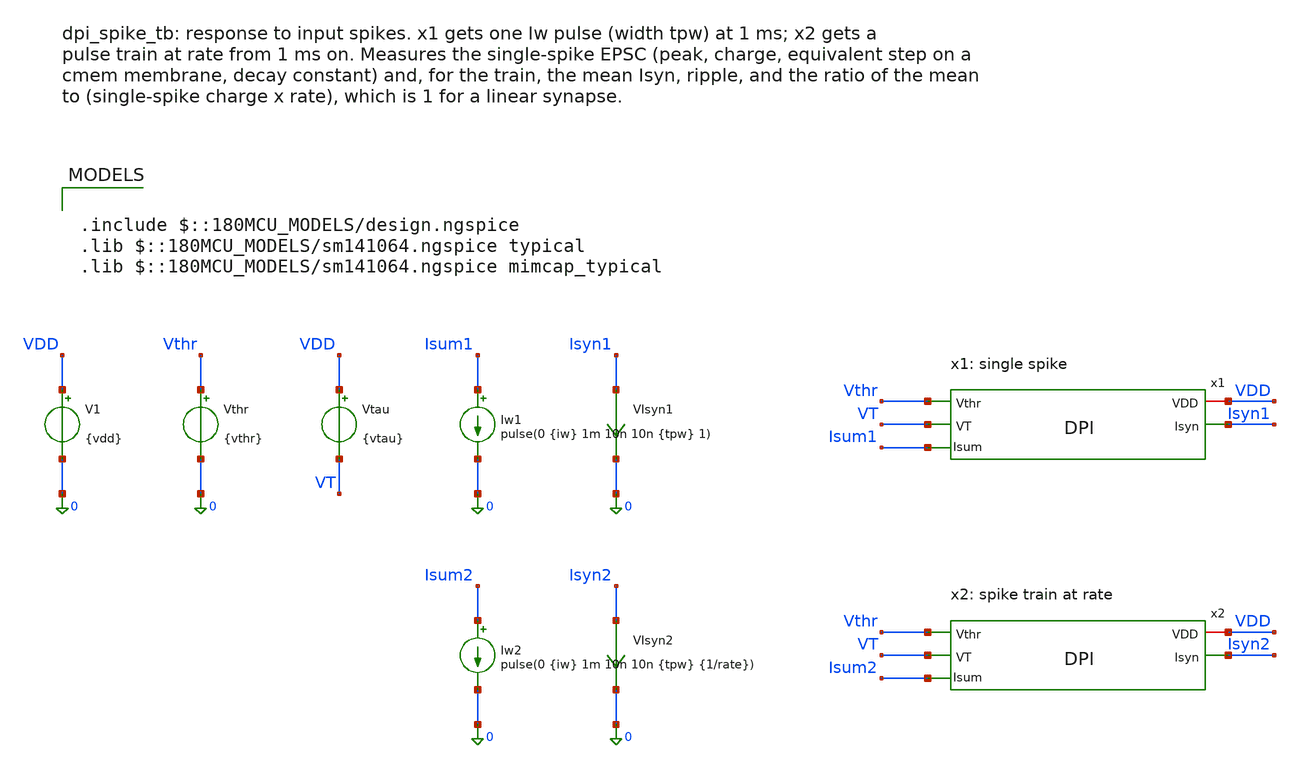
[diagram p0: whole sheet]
** sch_path: analog/testbenches/dpi/dpi_spike_tb.sch
**.subckt dpi_spike_tb
V1 VDD 0 {vdd}
Vthr Vthr 0 {vthr}
Vtau VDD VT {vtau}
Iw1 Isum1 0 pulse(0 {iw} 1m 10n 10n {tpw} 1)
VIsyn1 Isyn1 0 0
.save i(visyn1)
Iw2 Isum2 0 pulse(0 {iw} 1m 10n 10n {tpw} {1/rate})
VIsyn2 Isyn2 0 0
.save i(visyn2)
x1 VDD Vthr Isyn1 Isum1 VT DPI
x2 VDD Vthr Isyn2 Isum2 VT DPI
**** begin user architecture code


* Reference operating point (see analog/testbenches/README.md)
* cmem is only used to convert charge per spike into a membrane step (neuron_5khz Cmem)
.param vdd=3.3 vthr=2.9 vtau=0.40 iw=5n tpw=100u rate=1k cmem=0.86p
.csparam iw_c={iw}
.csparam tpw_c={tpw}
.csparam rate_c={rate}
.csparam cmem_c={cmem}
.control
  save all
  set wr_singlescale
  set wr_vecnames
  tran 0.5u 21m 0 1u
  let isyn1 = i(VIsyn1)
  let isyn2 = i(VIsyn2)

  * Single spike (x1)
  meas tran i_base find isyn1 at=0.9m
  meas tran ipk1 max isyn1 from=1m to=11m
  meas tran q1 integ isyn1 from=1m to=11m
  let q1 = q1 - i_base*10m
  let dv_mem = q1/cmem_c
  let t_end = 1m + tpw_c
  let l37 = i_base + 0.3679*(ipk1 - i_base)
  meas tran t37 when isyn1=$&l37 fall=1 td=$&t_end
  let tau_epsc = t37 - t_end

  * Spike train (x2), measured once settled
  meas tran iavg2 avg isyn2 from=11m to=21m
  meas tran imax2 max isyn2 from=11m to=21m
  meas tran imin2 min isyn2 from=11m to=21m
  let ripple = (imax2 - imin2)/iavg2
  let lin_rate = (iavg2 - i_base)/(q1*rate_c)
  let pk_ratio = imax2/ipk1

  echo RES ipk1=$&ipk1
  echo RES q1=$&q1
  echo RES dv_mem=$&dv_mem
  echo RES tau_epsc=$&tau_epsc
  echo RES iavg2=$&iavg2
  echo RES ripple=$&ripple
  echo RES lin_rate=$&lin_rate
  echo RES pk_ratio=$&pk_ratio

  wrdata dpi_spike.txt isyn1 isyn2
  if $?batchmode = 0
    plot isyn1 isyn2 title 'Single spike (isyn1) and spike train (isyn2)' ylabel 'Isyn (A)'
    plot Isum1 Isum2 title 'Inputs for both'
  end
.endc



.include $::180MCU_MODELS/design.ngspice
.lib $::180MCU_MODELS/sm141064.ngspice typical
.lib $::180MCU_MODELS/sm141064.ngspice mimcap_typical

**** end user architecture code
**.ends

* expanding   symbol:  DPI.sym # of pins=5
** sym_path: analog/neuron/DPI.sym
** sch_path: analog/neuron/DPI.sch
.subckt DPI VDD Vthr Isyn Isum VT
*.ipin Vthr
*.iopin VDD
*.opin Isyn
*.opin Isum
*.ipin VT
XM1 VDD Vthr Isum Isum nfet_03v3 L=0.28u W=0.22u nf=1 ad='int((nf+1)/2) * W/nf * 0.18u' as='int((nf+2)/2) * W/nf * 0.18u'
+ pd='2*int((nf+1)/2) * (W/nf + 0.18u)' ps='2*int((nf+2)/2) * (W/nf + 0.18u)' nrd='0.18u / W' nrs='0.18u / W'
+ sa=0 sb=0 sd=0 m=1
XM2 net1 net1 Isum Isum nfet_03v3 L=0.28u W=0.22u nf=1 ad='int((nf+1)/2) * W/nf * 0.18u' as='int((nf+2)/2) * W/nf * 0.18u'
+ pd='2*int((nf+1)/2) * (W/nf + 0.18u)' ps='2*int((nf+2)/2) * (W/nf + 0.18u)' nrd='0.18u / W' nrs='0.18u / W'
+ sa=0 sb=0 sd=0 m=1
XM3 net1 VT VDD VDD pfet_03v3 L=0.28u W=0.22u nf=1 ad='int((nf+1)/2) * W/nf * 0.18u' as='int((nf+2)/2) * W/nf * 0.18u'
+ pd='2*int((nf+1)/2) * (W/nf + 0.18u)' ps='2*int((nf+2)/2) * (W/nf + 0.18u)' nrd='0.18u / W' nrs='0.18u / W'
+ sa=0 sb=0 sd=0 m=1
XM4 Isyn net1 VDD VDD pfet_03v3 L=0.28u W=0.22u nf=1 ad='int((nf+1)/2) * W/nf * 0.18u' as='int((nf+2)/2) * W/nf * 0.18u'
+ pd='2*int((nf+1)/2) * (W/nf + 0.18u)' ps='2*int((nf+2)/2) * (W/nf + 0.18u)' nrd='0.18u / W' nrs='0.18u / W'
+ sa=0 sb=0 sd=0 m=1
C4 VDD net1 1p m=1
.ends

.end
